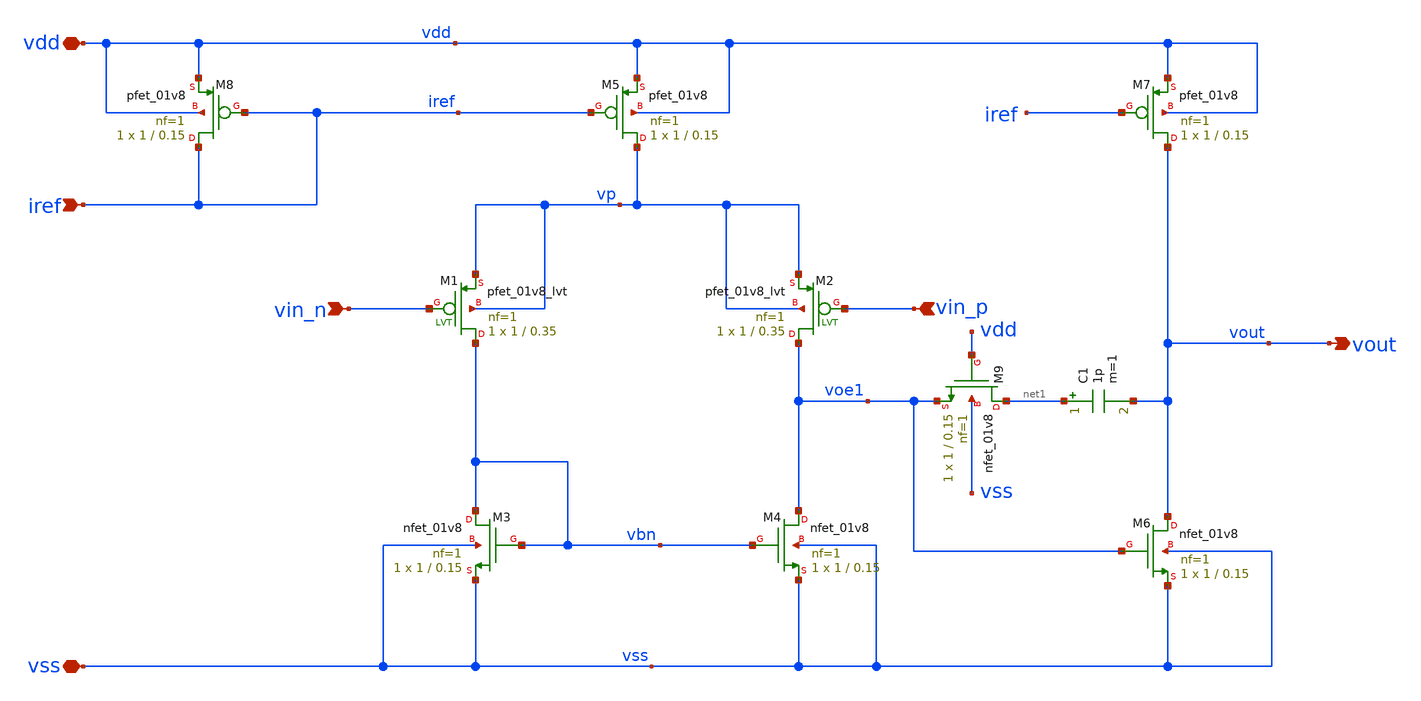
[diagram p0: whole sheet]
** sch_path: TpFinal/Simulacion Profesor /opamp.sch
**.subckt opamp vdd vss vin_n vin_p iref vout
*.iopin vdd
*.iopin vss
*.ipin vin_n
*.ipin vin_p
*.ipin iref
*.opin vout
XM3 vbn vbn vss vss sky130_fd_pr__nfet_01v8 L=0.15 W=1 nf=1 ad='W * 0.29' as='W * 0.29' pd='2 * (W + 0.29)'
+ ps='2 * (W + 0.29)' nrd='0.29 / W' nrs='0.29 / W' sa=0 sb=0 sd=0 mult=1 m=1
XM4 voe1 vbn vss vss sky130_fd_pr__nfet_01v8 L=0.15 W=1 nf=1 ad='W * 0.29' as='W * 0.29' pd='2 * (W + 0.29)'
+ ps='2 * (W + 0.29)' nrd='0.29 / W' nrs='0.29 / W' sa=0 sb=0 sd=0 mult=1 m=1
XM5 vp iref vdd vdd sky130_fd_pr__pfet_01v8 L=0.15 W=1 nf=1 ad='W * 0.29' as='W * 0.29' pd='2 * (W + 0.29)'
+ ps='2 * (W + 0.29)' nrd='0.29 / W' nrs='0.29 / W' sa=0 sb=0 sd=0 mult=1 m=1
XM7 vout iref vdd vdd sky130_fd_pr__pfet_01v8 L=0.15 W=1 nf=1 ad='W * 0.29' as='W * 0.29' pd='2 * (W + 0.29)'
+ ps='2 * (W + 0.29)' nrd='0.29 / W' nrs='0.29 / W' sa=0 sb=0 sd=0 mult=1 m=1
XM8 iref iref vdd vdd sky130_fd_pr__pfet_01v8 L=0.15 W=1 nf=1 ad='W * 0.29' as='W * 0.29' pd='2 * (W + 0.29)'
+ ps='2 * (W + 0.29)' nrd='0.29 / W' nrs='0.29 / W' sa=0 sb=0 sd=0 mult=1 m=1
XM9 net1 vdd voe1 vss sky130_fd_pr__nfet_01v8 L=0.15 W=1 nf=1 ad='W * 0.29' as='W * 0.29' pd='2 * (W + 0.29)'
+ ps='2 * (W + 0.29)' nrd='0.29 / W' nrs='0.29 / W' sa=0 sb=0 sd=0 mult=1 m=1
XM6 vout voe1 vss vss sky130_fd_pr__nfet_01v8 L=0.15 W=1 nf=1 ad='W * 0.29' as='W * 0.29' pd='2 * (W + 0.29)'
+ ps='2 * (W + 0.29)' nrd='0.29 / W' nrs='0.29 / W' sa=0 sb=0 sd=0 mult=1 m=1
XM1 vbn vin_n vp vp sky130_fd_pr__pfet_01v8_lvt L=0.35 W=1 nf=1 ad='int((nf+1)/2) * W/nf * 0.29' as='int((nf+2)/2) * W/nf * 0.29'
+ pd='2*int((nf+1)/2) * (W/nf + 0.29)' ps='2*int((nf+2)/2) * (W/nf + 0.29)' nrd='0.29 / W' nrs='0.29 / W'
+ sa=0 sb=0 sd=0 mult=1 m=1
XM2 voe1 vin_p vp vp sky130_fd_pr__pfet_01v8_lvt L=0.35 W=1 nf=1 ad='int((nf+1)/2) * W/nf * 0.29' as='int((nf+2)/2) * W/nf * 0.29'
+ pd='2*int((nf+1)/2) * (W/nf + 0.29)' ps='2*int((nf+2)/2) * (W/nf + 0.29)' nrd='0.29 / W' nrs='0.29 / W'
+ sa=0 sb=0 sd=0 mult=1 m=1
C1 net1 vout 1p m=1
**.ends
.end
